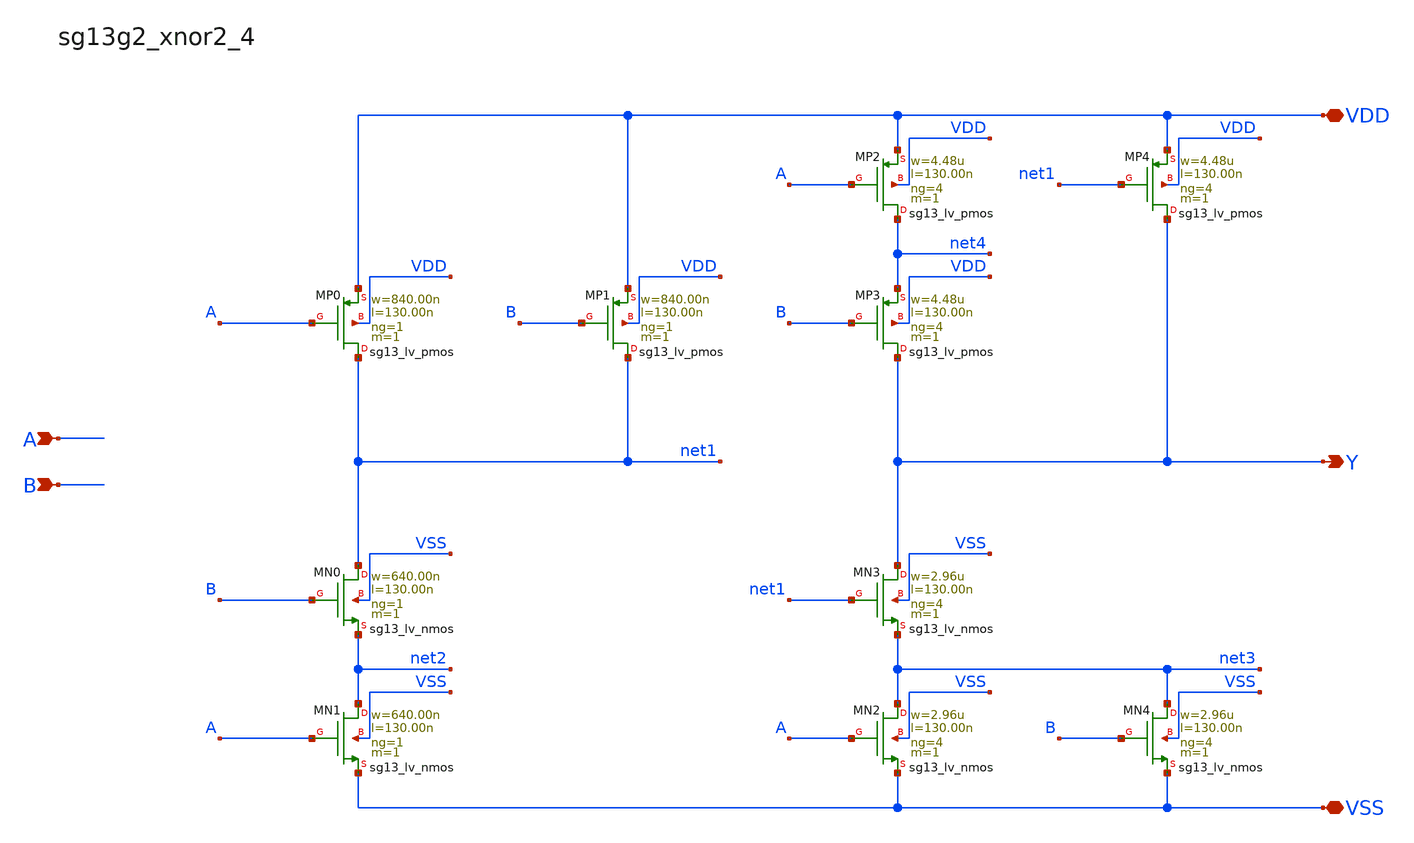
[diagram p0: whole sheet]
** sch_path: outputs/sg13g2_cells/cells/sg13g2_xnor2_4/sg13g2_xnor2_4.sch
**.subckt sg13g2_xnor2_4 Y A B VDD VSS
*.opin Y
*.ipin A
*.ipin B
*.iopin VDD
*.iopin VSS
XMP4 Y net1 VDD VDD sg13_lv_pmos w=4.48u l=130.00n ng=4 m=1 mm_ok=1
XMP3 Y B net4 VDD sg13_lv_pmos w=4.48u l=130.00n ng=4 m=1 mm_ok=1
XMP2 net4 A VDD VDD sg13_lv_pmos w=4.48u l=130.00n ng=4 m=1 mm_ok=1
XMP1 net1 B VDD VDD sg13_lv_pmos w=840.00n l=130.00n ng=1 m=1 mm_ok=1
XMP0 net1 A VDD VDD sg13_lv_pmos w=840.00n l=130.00n ng=1 m=1 mm_ok=1
XMN3 Y net1 net3 VSS sg13_lv_nmos w=2.96u l=130.00n ng=4 m=1 mm_ok=1
XMN1 net2 A VSS VSS sg13_lv_nmos w=640.00n l=130.00n ng=1 m=1 mm_ok=1
XMN0 net1 B net2 VSS sg13_lv_nmos w=640.00n l=130.00n ng=1 m=1 mm_ok=1
XMN4 net3 B VSS VSS sg13_lv_nmos w=2.96u l=130.00n ng=4 m=1 mm_ok=1
XMN2 net3 A VSS VSS sg13_lv_nmos w=2.96u l=130.00n ng=4 m=1 mm_ok=1
**.ends
.end
